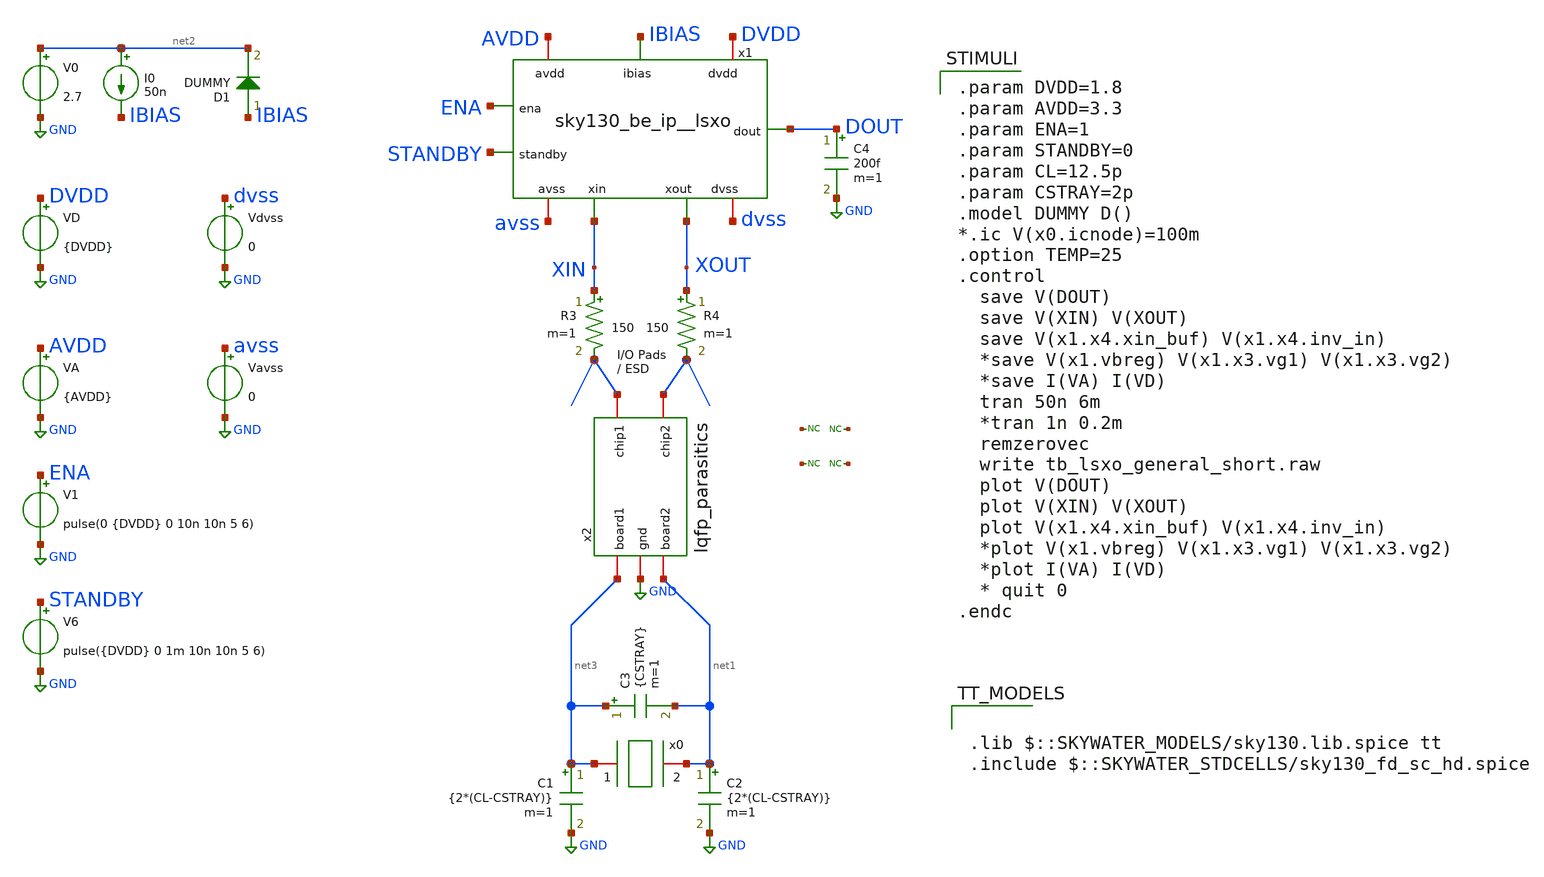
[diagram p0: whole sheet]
** sch_path: xschem/tb_man__sky130_be_ip__lsxo.sch

.lib $::SKYWATER_MODELS/sky130.lib.spice tt
.include $::SKYWATER_STDCELLS/sky130_fd_sc_hd.spice

**.subckt tb_man__sky130_be_ip__lsxo
VD DVDD GND {DVDD}
VA AVDD GND {AVDD}
C1 net3 GND {2*(CL-CSTRAY)} m=1
C2 net1 GND {2*(CL-CSTRAY)} m=1
C3 net3 net1 {CSTRAY} m=1
I0 net2 IBIAS 50n
C4 DOUT GND 200f m=1
V0 net2 GND 2.7
V6 STANDBY GND pulse({DVDD} 0 1m 10n 10n 5 6)
R3 XIN net4 150 m=1
R4 XOUT net5 150 m=1
x2 net5 net4 GND net3 net1 lqfp_parasitics
V1 ENA GND pulse(0 {DVDD} 0 10n 10n 5 6)
D1 IBIAS net2 DUMMY area=100
x1 AVDD avss DVDD dvss IBIAS ENA STANDBY DOUT XIN XOUT sky130_be_ip__lsxo
x0 net3 net1 xtal_iqd_125_1
Vdvss dvss GND 0
Vavss avss GND 0
* noconn #net6
* noconn #net7
* noconn #net8
* noconn #net9
**** begin user architecture code

.param DVDD=1.8
.param AVDD=3.3
.param ENA=1
.param STANDBY=0
.param CL=12.5p
.param CSTRAY=2p
.model DUMMY D()
*.ic V(x0.icnode)=100m
.option TEMP=25
.control
  save V(DOUT)
  save V(XIN) V(XOUT)
  save V(x1.x4.xin_buf) V(x1.x4.inv_in)
  *save V(x1.vbreg) V(x1.x3.vg1) V(x1.x3.vg2)
  *save I(VA) I(VD)
  tran 50n 6m
  *tran 1n 0.2m
  remzerovec
  write tb_lsxo_general_short.raw
  plot V(DOUT)
  plot V(XIN) V(XOUT)
  plot V(x1.x4.xin_buf) V(x1.x4.inv_in)
  *plot V(x1.vbreg) V(x1.x3.vg1) V(x1.x3.vg2)
  *plot I(VA) I(VD)
  * quit 0
.endc

**** end user architecture code
**.ends
.GLOBAL GND
.end
